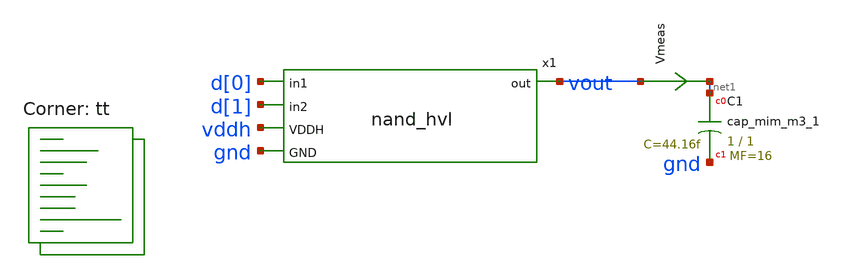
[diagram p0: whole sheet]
** sch_path: xschem/nand_hvl-tb.sch
**.subckt nand_hvl-tb
XC1 net1 gnd sky130_fd_pr__cap_mim_m3_1 W=1 L=1 MF=16 m=16
x1 d[0] d[1] vout vddh gnd nand_hvl
Vmeas vout net1 0
.save i(vmeas)
**** begin user architecture code
.lib $::SKYWATER_MODELS/sky130.lib.spice tt



  .option wnflag=1
  .option safecurrents
  ********************Static Voltage Sources***************************
  Vddh vddh gnd dc 5.5

  ********************Dynamic Voltage Sources***************************
  *******Calculation**********
  .param base_f=100e3 base_t={1/base_f} base_th={base_t/2} base_d={base_th}
  .param d2_th ={base_th} d2_t={2*d2_th}
  .param d1_th ={4*d2_th} d1_t={d0_th}
  .param d0_th ={4*d1_th} d0_t={4*d0_th}

  .param d20_d ={0} d21_d={1*d2_th} d22_d={2*d2_th} d23_d={3*d2_th}
  .param d10_d ={0} d11_d={1*d1_th} d12_d={2*d1_th} d13_d={3*d1_th}
  .param d00_d ={0} d01_d={1*d0_th} d02_d={2*d0_th} d03_d={3*d0_th}
  *******Signals**********
  .param vhi=5.5
  Vd00 d[0] gnd pulse(0 {vhi} {0} 1p 1p {10u} {20u})
  Vd01 d[1] gnd pulse(0 {vhi} {0} 1p 1p {20u} {40u})
  ********************Simulation Commands*****************************
  .control
     reset
     save all
     tran 1n 50u
     write nand_hvl-tb.raw
     set appendwrite
*    quit 0
  .endc



**** end user architecture code
**.ends

* expanding   symbol:  nand_hvl.sym # of pins=5
** sym_path: xschem/nand_hvl.sym
** sch_path: xschem/nand_hvl.sch
.subckt nand_hvl in1 in2 out VDDH GND
*.ipin in2
*.opin out
*.ipin VDDH
*.ipin GND
*.ipin in1
.param wp=0.42 wn=0.42 l=0.5
XM1 out in1 VDDH VDDH sky130_fd_pr__pfet_g5v0d10v5 L=l W=wp nf=1 ad='int((nf+1)/2) * W/nf * 0.29' as='int((nf+2)/2) * W/nf * 0.29'
+ pd='2*int((nf+1)/2) * (W/nf + 0.29)' ps='2*int((nf+2)/2) * (W/nf + 0.29)' nrd='0.29 / W' nrs='0.29 / W'
+ sa=0 sb=0 sd=0 mult=1 m=1
XM2 out in2 VDDH VDDH sky130_fd_pr__pfet_g5v0d10v5 L=l W=wp nf=1 ad='int((nf+1)/2) * W/nf * 0.29' as='int((nf+2)/2) * W/nf * 0.29'
+ pd='2*int((nf+1)/2) * (W/nf + 0.29)' ps='2*int((nf+2)/2) * (W/nf + 0.29)' nrd='0.29 / W' nrs='0.29 / W'
+ sa=0 sb=0 sd=0 mult=1 m=1
XM3 out in2 net1 GND sky130_fd_pr__nfet_g5v0d10v5 L=l W=wn nf=1 ad='int((nf+1)/2) * W/nf * 0.29' as='int((nf+2)/2) * W/nf * 0.29'
+ pd='2*int((nf+1)/2) * (W/nf + 0.29)' ps='2*int((nf+2)/2) * (W/nf + 0.29)' nrd='0.29 / W' nrs='0.29 / W'
+ sa=0 sb=0 sd=0 mult=1 m=1
XM4 net1 in1 GND GND sky130_fd_pr__nfet_g5v0d10v5 L=l W=wn nf=1 ad='int((nf+1)/2) * W/nf * 0.29' as='int((nf+2)/2) * W/nf * 0.29'
+ pd='2*int((nf+1)/2) * (W/nf + 0.29)' ps='2*int((nf+2)/2) * (W/nf + 0.29)' nrd='0.29 / W' nrs='0.29 / W'
+ sa=0 sb=0 sd=0 mult=1 m=1
.ends

.end
